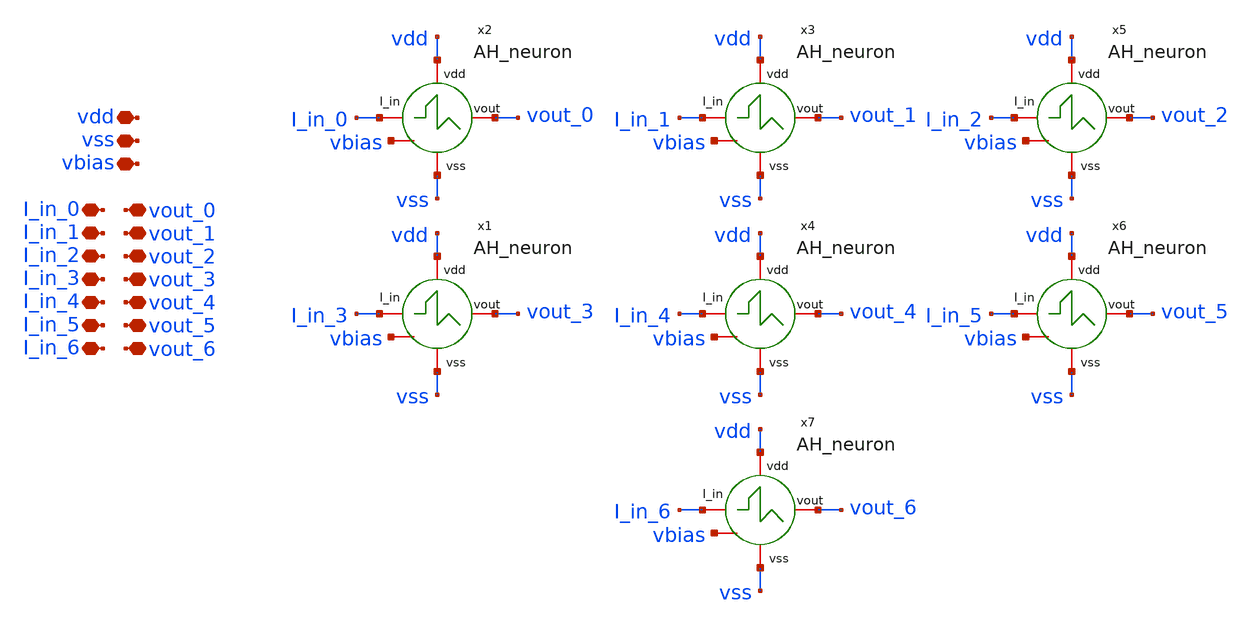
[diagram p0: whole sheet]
** sch_path: designs/libs/core_AH_neuron_arr/AH_neuron_arr.sch
**.subckt AH_neuron_arr vdd vss I_in_0 vout_0 I_in_6 vout_6 I_in_1 vout_1 I_in_2 vout_2 I_in_3
*+ vout_3 I_in_4 vout_4 I_in_5 vout_5 vbias
*.iopin vdd
*.iopin vss
*.iopin I_in_0
*.iopin vout_0
*.iopin I_in_6
*.iopin vout_6
*.iopin I_in_1
*.iopin vout_1
*.iopin I_in_2
*.iopin vout_2
*.iopin I_in_3
*.iopin vout_3
*.iopin I_in_4
*.iopin vout_4
*.iopin I_in_5
*.iopin vout_5
*.iopin vbias
x1 vdd I_in_3 vout_3 vss vbias AH_neuron
x2 vdd I_in_0 vout_0 vss vbias AH_neuron
x3 vdd I_in_1 vout_1 vss vbias AH_neuron
x4 vdd I_in_4 vout_4 vss vbias AH_neuron
x5 vdd I_in_2 vout_2 vss vbias AH_neuron
x6 vdd I_in_5 vout_5 vss vbias AH_neuron
x7 vdd I_in_6 vout_6 vss vbias AH_neuron
**.ends
.end
